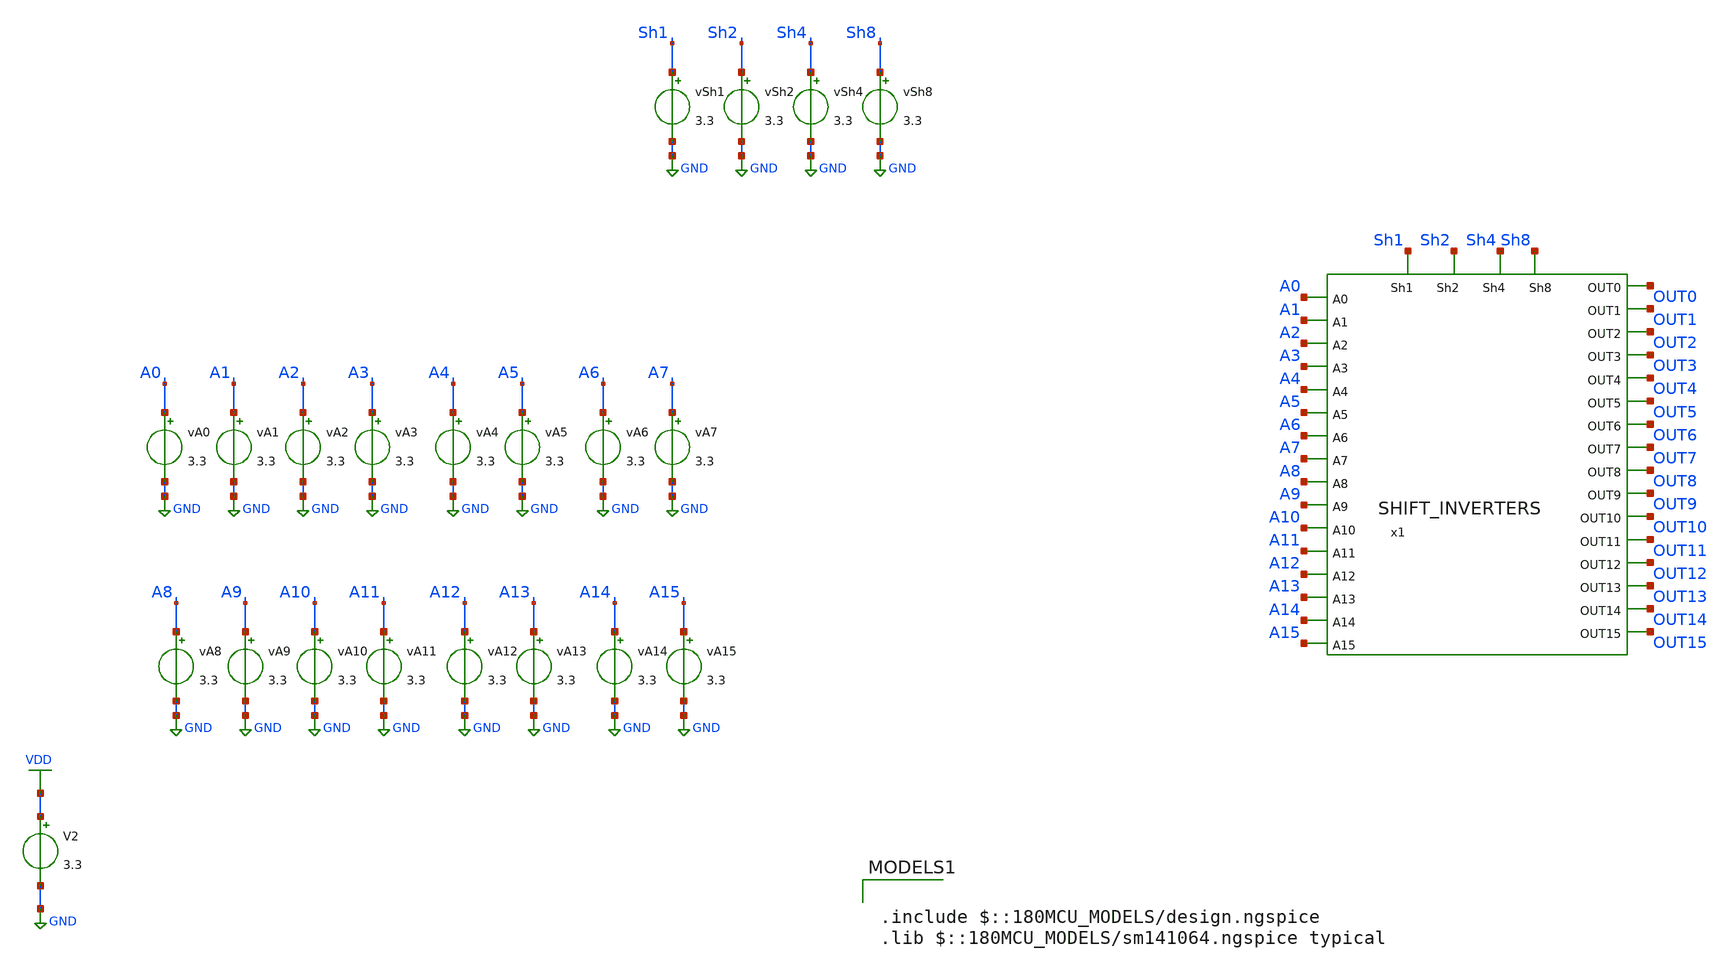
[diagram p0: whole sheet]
** sch_path: tbs/shift_tb_1_to_6.sch
**.subckt shift_tb_1_to_6
x1 OUT0 Sh1 OUT1 OUT2 Sh2 OUT3 OUT4 A0 OUT5 A1 OUT6 Sh4 OUT7 OUT8 A2 A3 OUT9 OUT10 OUT11 Sh8 OUT12
+ A4 OUT13 A5 A6 OUT14 A7 OUT15 A8 A9 A10 A11 A12 A13 A14 A15 SHIFT_INVERTERS
vA0 A0 GND 3.3
vA1 A1 GND 3.3
vA2 A2 GND 3.3
vA3 A3 GND 3.3
vA4 A4 GND 3.3
vA5 A5 GND 3.3
vA6 A6 GND 3.3
vA7 A7 GND 3.3
vA8 A8 GND 3.3
vA9 A9 GND 3.3
vA10 A10 GND 3.3
vA11 A11 GND 3.3
vA12 A12 GND 3.3
vA13 A13 GND 3.3
vA14 A14 GND 3.3
vA15 A15 GND 3.3
vSh1 Sh1 GND 3.3
vSh2 Sh2 GND 3.3
vSh4 Sh4 GND 3.3
vSh8 Sh8 GND 3.3
V2 VDD GND 3.3
**** begin user architecture code

.include $::180MCU_MODELS/design.ngspice
.lib $::180MCU_MODELS/sm141064.ngspice typical



.control
let vlow = 0
let vhigh = 3.3
* A = 1010101010101010 = 43690
alter VA15 = $&vhigh
alter VA14 = $&vlow
alter VA13 = $&vhigh
alter VA12 = $&vlow
alter VA11 = $&vhigh
alter VA10 = $&vlow
alter VA9  = $&vhigh
alter VA8  = $&vlow
alter VA7  = $&vhigh
alter VA6  = $&vlow
alter VA5  = $&vhigh
alter VA4  = $&vlow
alter VA3  = $&vhigh
alter VA2  = $&vlow
alter VA1  = $&vhigh
alter VA0  = $&vlow

* --- SHIFT 1 (0001) ---
alter vSh8 = $&vlow
alter vSh4 = $&vlow
alter vSh2 = $&vlow
alter vSh1 = $&vhigh

tran 1n 40n

meas tran v1_0  find v(OUT0)  at=30n
meas tran v1_1  find v(OUT1)  at=30n
meas tran v1_2  find v(OUT2)  at=30n
meas tran v1_3  find v(OUT3)  at=30n
meas tran v1_4  find v(OUT4)  at=30n
meas tran v1_5  find v(OUT5)  at=30n
meas tran v1_6  find v(OUT6)  at=30n
meas tran v1_7  find v(OUT7)  at=30n
meas tran v1_8  find v(OUT8)  at=30n
meas tran v1_9  find v(OUT9)  at=30n
meas tran v1_10 find v(OUT10) at=30n
meas tran v1_11 find v(OUT11) at=30n
meas tran v1_12 find v(OUT12) at=30n
meas tran v1_13 find v(OUT13) at=30n
meas tran v1_14 find v(OUT14) at=30n
meas tran v1_15 find v(OUT15) at=30n

let res1 = 0
if v1_0 > 1.6
  let res1 = res1 + 1
end
if v1_1 > 1.6
  let res1 = res1 + 2
end
if v1_2 > 1.6
  let res1 = res1 + 4
end
if v1_3 > 1.6
  let res1 = res1 + 8
end
if v1_4 > 1.6
  let res1 = res1 + 16
end
if v1_5 > 1.6
  let res1 = res1 + 32
end
if v1_6 > 1.6
  let res1 = res1 + 64
end
if v1_7 > 1.6
  let res1 = res1 + 128
end
if v1_8 > 1.6
  let res1 = res1 + 256
end
if v1_9 > 1.6
  let res1 = res1 + 512
end
if v1_10 > 1.6
  let res1 = res1 + 1024
end
if v1_11 > 1.6
  let res1 = res1 + 2048
end
if v1_12 > 1.6
  let res1 = res1 + 4096
end
if v1_13 > 1.6
  let res1 = res1 + 8192
end
if v1_14 > 1.6
  let res1 = res1 + 16384
end
if v1_15 > 1.6
  let res1 = res1 + 32768
end
echo 1_gives_21844
print res1
* --- SHIFT 2 (0010) ---
alter vSh1 = $&vlow
alter vSh2 = $&vhigh

tran 1n 40n

meas tran v2_0  find v(OUT0)  at=30n
meas tran v2_1  find v(OUT1)  at=30n
meas tran v2_2  find v(OUT2)  at=30n
meas tran v2_3  find v(OUT3)  at=30n
meas tran v2_4  find v(OUT4)  at=30n
meas tran v2_5  find v(OUT5)  at=30n
meas tran v2_6  find v(OUT6)  at=30n
meas tran v2_7  find v(OUT7)  at=30n
meas tran v2_8  find v(OUT8)  at=30n
meas tran v2_9  find v(OUT9)  at=30n
meas tran v2_10 find v(OUT10) at=30n
meas tran v2_11 find v(OUT11) at=30n
meas tran v2_12 find v(OUT12) at=30n
meas tran v2_13 find v(OUT13) at=30n
meas tran v2_14 find v(OUT14) at=30n
meas tran v2_15 find v(OUT15) at=30n

let res2 = 0
if v2_0 > 1.6
  let res2 = res2 + 1
end
if v2_1 > 1.6
  let res2 = res2 + 2
end
if v2_2 > 1.6
  let res2 = res2 + 4
end
if v2_3 > 1.6
  let res2 = res2 + 8
end
if v2_4 > 1.6
  let res2 = res2 + 16
end
if v2_5 > 1.6
  let res2 = res2 + 32
end
if v2_6 > 1.6
  let res2 = res2 + 64
end
if v2_7 > 1.6
  let res2 = res2 + 128
end
if v2_8 > 1.6
  let res2 = res2 + 256
end
if v2_9 > 1.6
  let res2 = res2 + 512
end
if v2_10 > 1.6
  let res2 = res2 + 1024
end
if v2_11 > 1.6
  let res2 = res2 + 2048
end
if v2_12 > 1.6
  let res2 = res2 + 4096
end
if v2_13 > 1.6
  let res2 = res2 + 8192
end
if v2_14 > 1.6
  let res2 = res2 + 16384
end
if v2_15 > 1.6
  let res2 = res2 + 32768
end
echo 2_gives_43688
print res2
* --- SHIFT 3 (0011) ---
alter vSh1 = $&vhigh
alter vSh2 = $&vhigh

tran 1n 40n

meas tran v3_0  find v(OUT0)  at=30n
meas tran v3_1  find v(OUT1)  at=30n
meas tran v3_2  find v(OUT2)  at=30n
meas tran v3_3  find v(OUT3)  at=30n
meas tran v3_4  find v(OUT4)  at=30n
meas tran v3_5  find v(OUT5)  at=30n
meas tran v3_6  find v(OUT6)  at=30n
meas tran v3_7  find v(OUT7)  at=30n
meas tran v3_8  find v(OUT8)  at=30n
meas tran v3_9  find v(OUT9)  at=30n
meas tran v3_10 find v(OUT10) at=30n
meas tran v3_11 find v(OUT11) at=30n
meas tran v3_12 find v(OUT12) at=30n
meas tran v3_13 find v(OUT13) at=30n
meas tran v3_14 find v(OUT14) at=30n
meas tran v3_15 find v(OUT15) at=30n

let res3 = 0
if v3_0 > 1.6
  let res3 = res3 + 1
end
if v3_1 > 1.6
  let res3 = res3 + 2
end
if v3_2 > 1.6
  let res3 = res3 + 4
end
if v3_3 > 1.6
  let res3 = res3 + 8
end
if v3_4 > 1.6
  let res3 = res3 + 16
end
if v3_5 > 1.6
  let res3 = res3 + 32
end
if v3_6 > 1.6
  let res3 = res3 + 64
end
if v3_7 > 1.6
  let res3 = res3 + 128
end
if v3_8 > 1.6
  let res3 = res3 + 256
end
if v3_9 > 1.6
  let res3 = res3 + 512
end
if v3_10 > 1.6
  let res3 = res3 + 1024
end
if v3_11 > 1.6
  let res3 = res3 + 2048
end
if v3_12 > 1.6
  let res3 = res3 + 4096
end
if v3_13 > 1.6
  let res3 = res3 + 8192
end
if v3_14 > 1.6
  let res3 = res3 + 16384
end
if v3_15 > 1.6
  let res3 = res3 + 32768
end
echo 3_gives_21840
print res3
* --- SHIFT 4 (0100) ---
alter vSh1 = $&vlow
alter vSh2 = $&vlow
alter vSh4 = $&vhigh

tran 1n 40n

meas tran v4_0  find v(OUT0)  at=30n
meas tran v4_1  find v(OUT1)  at=30n
meas tran v4_2  find v(OUT2)  at=30n
meas tran v4_3  find v(OUT3)  at=30n
meas tran v4_4  find v(OUT4)  at=30n
meas tran v4_5  find v(OUT5)  at=30n
meas tran v4_6  find v(OUT6)  at=30n
meas tran v4_7  find v(OUT7)  at=30n
meas tran v4_8  find v(OUT8)  at=30n
meas tran v4_9  find v(OUT9)  at=30n
meas tran v4_10 find v(OUT10) at=30n
meas tran v4_11 find v(OUT11) at=30n
meas tran v4_12 find v(OUT12) at=30n
meas tran v4_13 find v(OUT13) at=30n
meas tran v4_14 find v(OUT14) at=30n
meas tran v4_15 find v(OUT15) at=30n

let res4 = 0
if v4_0 > 1.6
  let res4 = res4 + 1
end
if v4_1 > 1.6
  let res4 = res4 + 2
end
if v4_2 > 1.6
  let res4 = res4 + 4
end
if v4_3 > 1.6
  let res4 = res4 + 8
end
if v4_4 > 1.6
  let res4 = res4 + 16
end
if v4_5 > 1.6
  let res4 = res4 + 32
end
if v4_6 > 1.6
  let res4 = res4 + 64
end
if v4_7 > 1.6
  let res4 = res4 + 128
end
if v4_8 > 1.6
  let res4 = res4 + 256
end
if v4_9 > 1.6
  let res4 = res4 + 512
end
if v4_10 > 1.6
  let res4 = res4 + 1024
end
if v4_11 > 1.6
  let res4 = res4 + 2048
end
if v4_12 > 1.6
  let res4 = res4 + 4096
end
if v4_13 > 1.6
  let res4 = res4 + 8192
end
if v4_14 > 1.6
  let res4 = res4 + 16384
end
if v4_15 > 1.6
  let res4 = res4 + 32768
end
echo 4_gives_43680
print res4
* --- SHIFT 5 (0101) ---
alter vSh8 = $&vlow
alter vSh4 = $&vhigh
alter vSh2 = $&vlow
alter vSh1 = $&vhigh

tran 1n 40n

meas tran v5_0  find v(OUT0)  at=30n
meas tran v5_1  find v(OUT1)  at=30n
meas tran v5_2  find v(OUT2)  at=30n
meas tran v5_3  find v(OUT3)  at=30n
meas tran v5_4  find v(OUT4)  at=30n
meas tran v5_5  find v(OUT5)  at=30n
meas tran v5_6  find v(OUT6)  at=30n
meas tran v5_7  find v(OUT7)  at=30n
meas tran v5_8  find v(OUT8)  at=30n
meas tran v5_9  find v(OUT9)  at=30n
meas tran v5_10 find v(OUT10) at=30n
meas tran v5_11 find v(OUT11) at=30n
meas tran v5_12 find v(OUT12) at=30n
meas tran v5_13 find v(OUT13) at=30n
meas tran v5_14 find v(OUT14) at=30n
meas tran v5_15 find v(OUT15) at=30n

let res5 = 0
if v5_0 > 1.6
  let res5 = res5 + 1
end
if v5_1 > 1.6
  let res5 = res5 + 2
end
if v5_2 > 1.6
  let res5 = res5 + 4
end
if v5_3 > 1.6
  let res5 = res5 + 8
end
if v5_4 > 1.6
  let res5 = res5 + 16
end
if v5_5 > 1.6
  let res5 = res5 + 32
end
if v5_6 > 1.6
  let res5 = res5 + 64
end
if v5_7 > 1.6
  let res5 = res5 + 128
end
if v5_8 > 1.6
  let res5 = res5 + 256
end
if v5_9 > 1.6
  let res5 = res5 + 512
end
if v5_10 > 1.6
  let res5 = res5 + 1024
end
if v5_11 > 1.6
  let res5 = res5 + 2048
end
if v5_12 > 1.6
  let res5 = res5 + 4096
end
if v5_13 > 1.6
  let res5 = res5 + 8192
end
if v5_14 > 1.6
  let res5 = res5 + 16384
end
if v5_15 > 1.6
  let res5 = res5 + 32768
end
echo 5_gives_21824
print res5

* --- SHIFT 6 (0110) ---
alter vSh1 = $&vlow
alter vSh2 = $&vhigh
tran 1n 40n

meas tran v6_0  find v(OUT0)  at=30n
meas tran v6_1  find v(OUT1)  at=30n
meas tran v6_2  find v(OUT2)  at=30n
meas tran v6_3  find v(OUT3)  at=30n
meas tran v6_4  find v(OUT4)  at=30n
meas tran v6_5  find v(OUT5)  at=30n
meas tran v6_6  find v(OUT6)  at=30n
meas tran v6_7  find v(OUT7)  at=30n
meas tran v6_8  find v(OUT8)  at=30n
meas tran v6_9  find v(OUT9)  at=30n
meas tran v6_10 find v(OUT10) at=30n
meas tran v6_11 find v(OUT11) at=30n
meas tran v6_12 find v(OUT12) at=30n
meas tran v6_13 find v(OUT13) at=30n
meas tran v6_14 find v(OUT14) at=30n
meas tran v6_15 find v(OUT15) at=30n

let res6 = 0
if v6_0 > 1.6
  let res6 = res6 + 1
end
if v6_1 > 1.6
  let res6 = res6 + 2
end
if v6_2 > 1.6
  let res6 = res6 + 4
end
if v6_3 > 1.6
  let res6 = res6 + 8
end
if v6_4 > 1.6
  let res6 = res6 + 16
end
if v6_5 > 1.6
  let res6 = res6 + 32
end
if v6_6 > 1.6
  let res6 = res6 + 64
end
if v6_7 > 1.6
  let res6 = res6 + 128
end
if v6_8 > 1.6
  let res6 = res6 + 256
end
if v6_9 > 1.6
  let res6 = res6 + 512
end
if v6_10 > 1.6
  let res6 = res6 + 1024
end
if v6_11 > 1.6
  let res6 = res6 + 2048
end
if v6_12 > 1.6
  let res6 = res6 + 4096
end
if v6_13 > 1.6
  let res6 = res6 + 8192
end
if v6_14 > 1.6
  let res6 = res6 + 16384
end
if v6_15 > 1.6
  let res6 = res6 + 32768
end
echo 6_gives_43648
print res6
.endc


**** end user architecture code
**.ends
.GLOBAL GND
.GLOBAL VDD
.end
